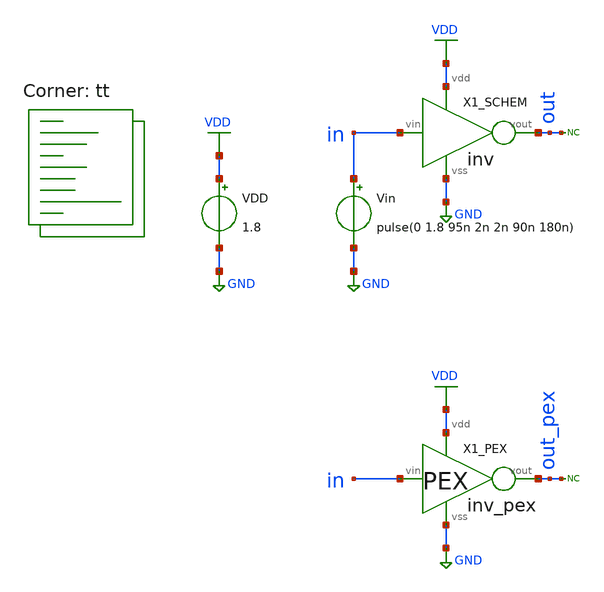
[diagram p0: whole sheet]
** sch_path: xsch/tb/inv/tb_pex_inv_tran.sch
**.subckt tb_pex_inv_tran
Vin in GND pulse(0 1.8 95n 2n 2n 90n 180n)
VDD VDD GND 1.8
* noconn out
X1_SCHEM in out VDD GND inv
* noconn out_pex
X1_PEX in out_pex VDD GND inv_pex
**** begin user architecture code



* control language script

.control
set xbrushwidth=2

tran 100p 500n               ; simulation command 1

plot v(in) v(out) v(out_pex)

reset

dc vin 0 2 0.01              ; simulation command 2

plot v(out) v(out_pex)

.endc
.end



.lib $::SKYWATER_MODELS/sky130.lib.spice tt


.include ~/projects/tt06_555/xsch/ip/logic/inv/inv_pex.spice


**** end user architecture code
**.ends
.GLOBAL VDD
.GLOBAL GND
.end
